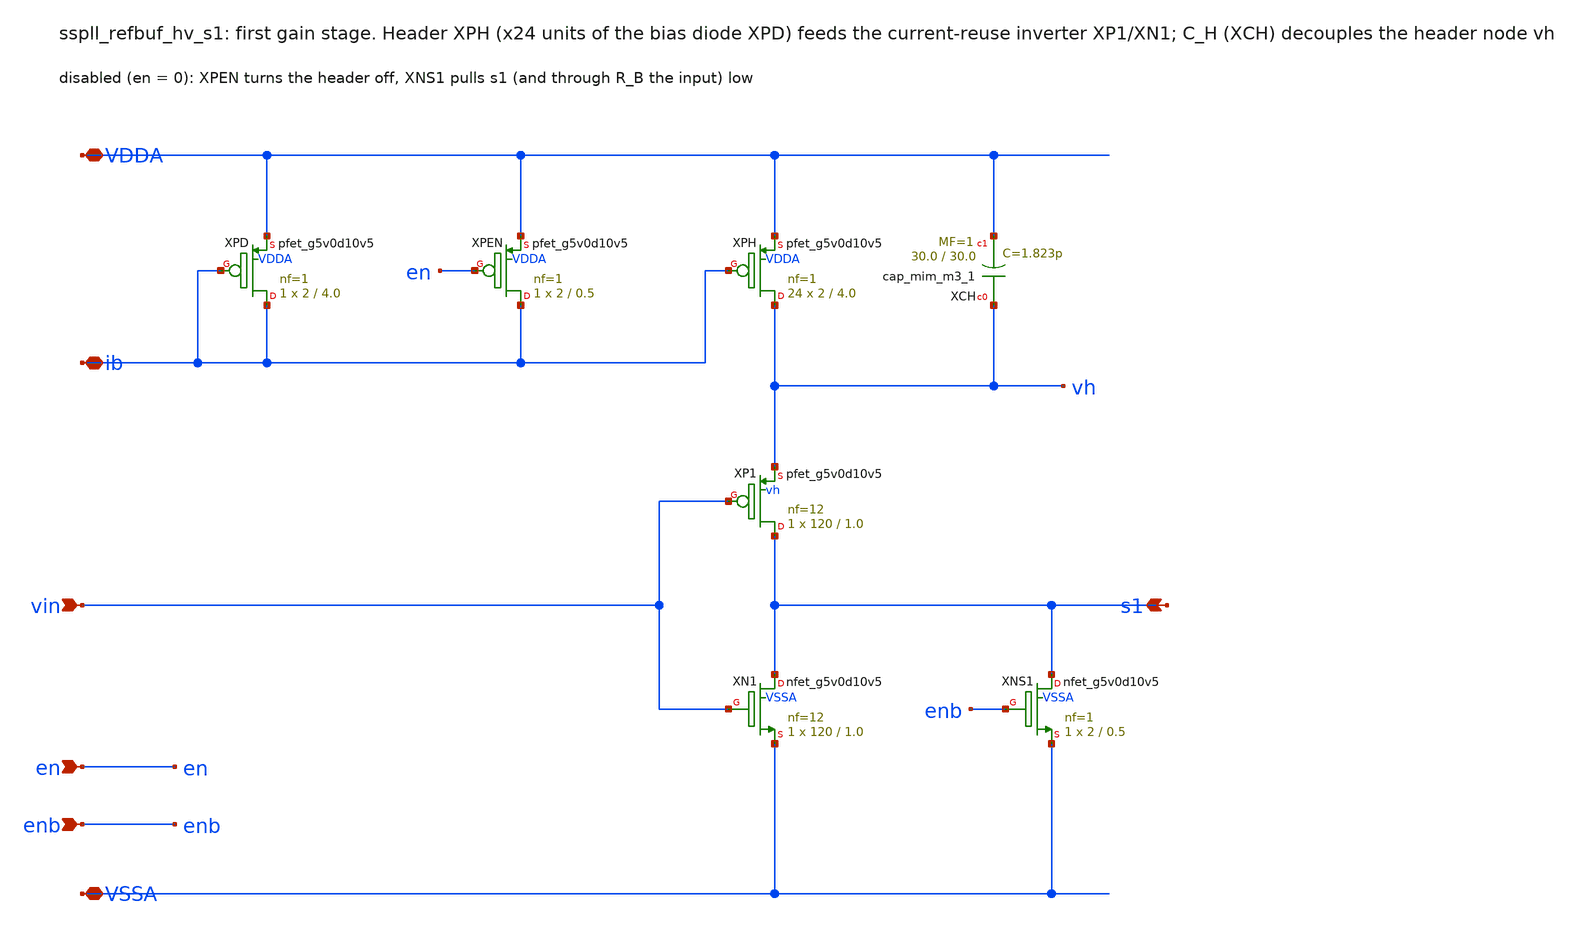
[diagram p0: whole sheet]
** sch_path: xschem/refbuf_hv/sspll_refbuf_hv_s1.sch
**.subckt sspll_refbuf_hv_s1 VDDA VSSA ib vin s1 en enb
*.iopin VDDA
*.iopin VSSA
*.iopin ib
*.ipin vin
*.opin s1
*.ipin en
*.ipin enb
XXPD ib ib VDDA VDDA sky130_fd_pr__pfet_g5v0d10v5 L=4.0 W=2 nf=1 ad='int((nf+1)/2) * W/nf * 0.29' as='int((nf+2)/2) * W/nf * 0.29'
+ pd='2*int((nf+1)/2) * (W/nf + 0.29)' ps='2*int((nf+2)/2) * (W/nf + 0.29)' nrd='0.29 / W' nrs='0.29 / W'
+ sa=0 sb=0 sd=0 mult=1 m=1
XXPEN ib en VDDA VDDA sky130_fd_pr__pfet_g5v0d10v5 L=0.5 W=2 nf=1 ad='int((nf+1)/2) * W/nf * 0.29' as='int((nf+2)/2) * W/nf * 0.29'
+ pd='2*int((nf+1)/2) * (W/nf + 0.29)' ps='2*int((nf+2)/2) * (W/nf + 0.29)' nrd='0.29 / W' nrs='0.29 / W'
+ sa=0 sb=0 sd=0 mult=1 m=1
XXPH vh ib VDDA VDDA sky130_fd_pr__pfet_g5v0d10v5 L=4.0 W=2 nf=1 ad='int((nf+1)/2) * W/nf * 0.29' as='int((nf+2)/2) * W/nf * 0.29'
+ pd='2*int((nf+1)/2) * (W/nf + 0.29)' ps='2*int((nf+2)/2) * (W/nf + 0.29)' nrd='0.29 / W' nrs='0.29 / W'
+ sa=0 sb=0 sd=0 mult=24 m=24
XXCH vh VDDA sky130_fd_pr__cap_mim_m3_1 W=30.0 L=30.0 MF=1 m=1
XXP1 s1 vin vh vh sky130_fd_pr__pfet_g5v0d10v5 L=1.0 W=120 nf=12 ad='int((nf+1)/2) * W/nf * 0.29' as='int((nf+2)/2) * W/nf * 0.29'
+ pd='2*int((nf+1)/2) * (W/nf + 0.29)' ps='2*int((nf+2)/2) * (W/nf + 0.29)' nrd='0.29 / W' nrs='0.29 / W'
+ sa=0 sb=0 sd=0 mult=1 m=1
XXN1 s1 vin VSSA VSSA sky130_fd_pr__nfet_g5v0d10v5 L=1.0 W=120 nf=12 ad='int((nf+1)/2) * W/nf * 0.29'
+ as='int((nf+2)/2) * W/nf * 0.29' pd='2*int((nf+1)/2) * (W/nf + 0.29)' ps='2*int((nf+2)/2) * (W/nf + 0.29)'
+ nrd='0.29 / W' nrs='0.29 / W' sa=0 sb=0 sd=0 mult=1 m=1
XXNS1 s1 enb VSSA VSSA sky130_fd_pr__nfet_g5v0d10v5 L=0.5 W=2 nf=1 ad='int((nf+1)/2) * W/nf * 0.29' as='int((nf+2)/2) * W/nf * 0.29'
+ pd='2*int((nf+1)/2) * (W/nf + 0.29)' ps='2*int((nf+2)/2) * (W/nf + 0.29)' nrd='0.29 / W' nrs='0.29 / W'
+ sa=0 sb=0 sd=0 mult=1 m=1
**.ends
.end
